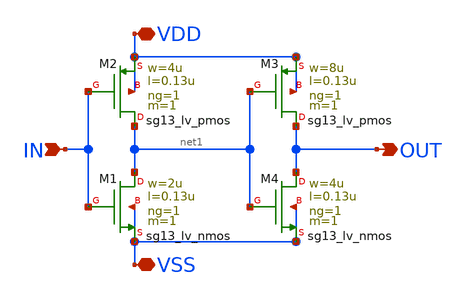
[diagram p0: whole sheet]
** sch_path: SSDOR_1.2V_v3/components/ring_osc/inv_buff.sch
**.subckt inv_buff IN VDD VSS OUT
*.ipin IN
*.iopin VDD
*.iopin VSS
*.opin OUT
XM1 net1 IN VSS VSS sg13_lv_nmos w=2u l=0.13u ng=1 m=1 mm_ok=1
XM2 net1 IN VDD VDD sg13_lv_pmos w=4u l=0.13u ng=1 m=1 mm_ok=1
XM3 OUT net1 VDD VDD sg13_lv_pmos w=8u l=0.13u ng=1 m=1 mm_ok=1
XM4 OUT net1 VSS VSS sg13_lv_nmos w=4u l=0.13u ng=1 m=1 mm_ok=1
**.ends
.end
